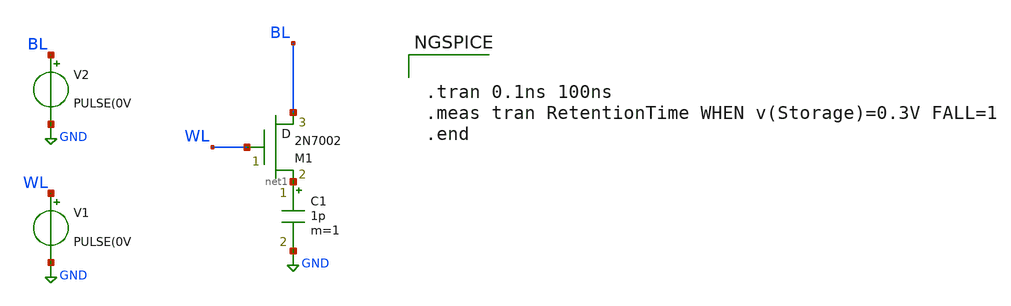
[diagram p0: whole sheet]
** sch_path: 1T1C_eDRAM.sch
**.subckt 1T1C_eDRAM
M1 BL WL net1 M2N7002 m=1
C1 net1 GND 1p m=1
V1 WL GND PULSE(0V
V2 BL GND PULSE(0V
**** begin user architecture code


.tran 0.1ns 100ns
.meas tran RetentionTime WHEN v(Storage)=0.3V FALL=1
.end


**** end user architecture code
**.ends
.GLOBAL GND
.end
